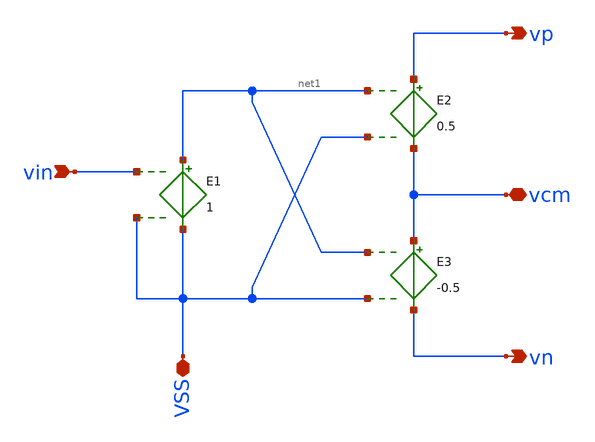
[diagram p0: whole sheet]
** sch_path: xschem_library/devices/single2cm.sch
**.subckt single2cm vin vn vcm vp VSS
*.ipin vin
*.opin vn
*.iopin vcm
*.opin vp
*.iopin VSS
E3 vcm vn net1 VSS -0.5
E2 vp vcm net1 VSS 0.5
E1 net1 VSS vin VSS 1
**.ends
.end
